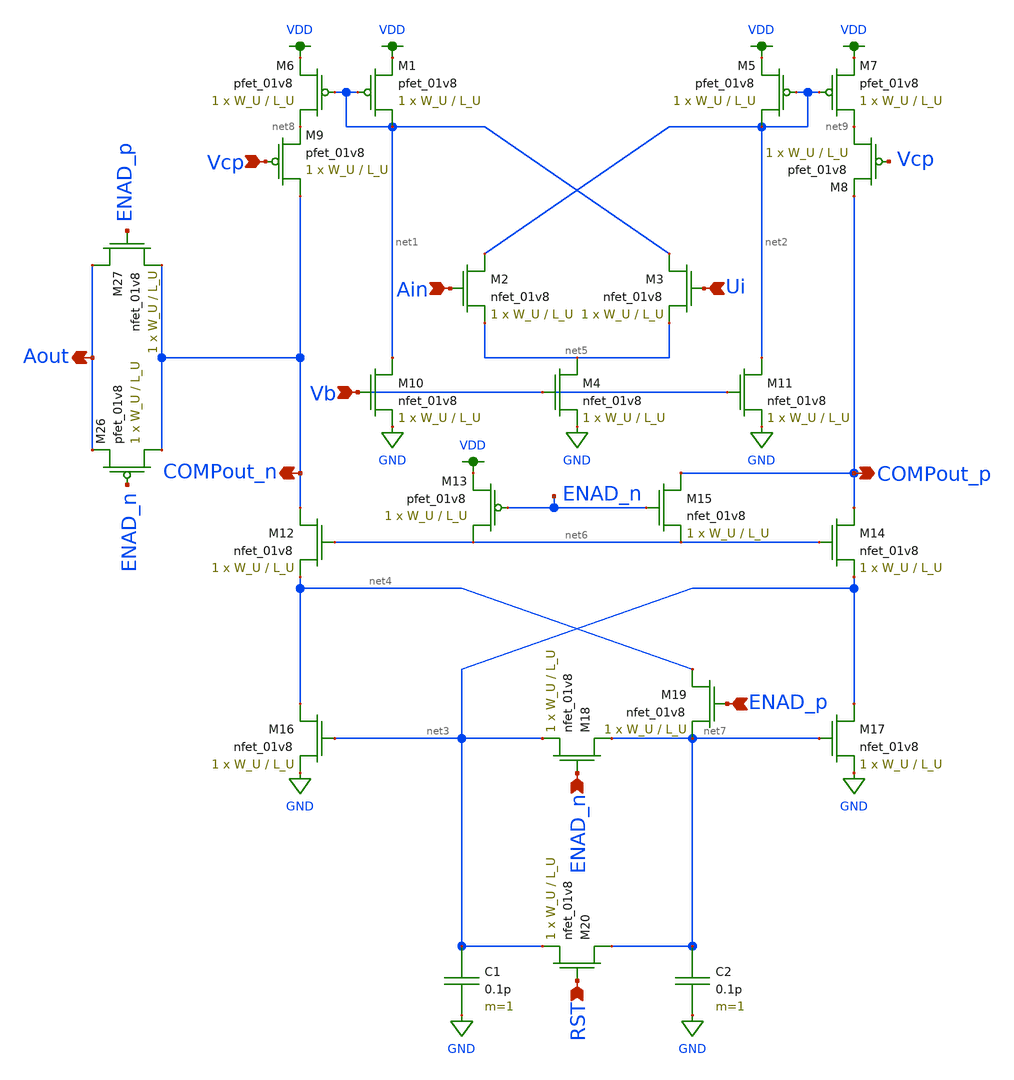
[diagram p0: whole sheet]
** sch_path: schematics/comp_pretty.sch
**.subckt comp_pretty Ain Vcp Vb Aout COMPout_n COMPout_p ENAD_n RST Ui ENAD_p
*.ipin Ain
*.ipin Vcp
*.ipin Vb
*.opin Aout
*.opin COMPout_n
*.opin COMPout_p
*.ipin ENAD_n
*.ipin RST
*.ipin Ui
*.ipin ENAD_p
XM1 net1 net1 VDD VDD sky130_fd_pr__pfet_01v8 L=L_U W=W_U nf=1 ad='int((nf+1)/2) * W/nf * 0.29' as='int((nf+2)/2) * W/nf * 0.29'
+ pd='2*int((nf+1)/2) * (W/nf + 0.29)' ps='2*int((nf+2)/2) * (W/nf + 0.29)' nrd='0.29 / W' nrs='0.29 / W'
+ sa=0 sb=0 sd=0 mult=1 m=1
XM2 net2 Ain net5 GND sky130_fd_pr__nfet_01v8 L=L_U W=W_U nf=1 ad='int((nf+1)/2) * W/nf * 0.29' as='int((nf+2)/2) * W/nf * 0.29'
+ pd='2*int((nf+1)/2) * (W/nf + 0.29)' ps='2*int((nf+2)/2) * (W/nf + 0.29)' nrd='0.29 / W' nrs='0.29 / W'
+ sa=0 sb=0 sd=0 mult=1 m=1
XM3 net1 Ui net5 GND sky130_fd_pr__nfet_01v8 L=L_U W=W_U nf=1 ad='int((nf+1)/2) * W/nf * 0.29' as='int((nf+2)/2) * W/nf * 0.29'
+ pd='2*int((nf+1)/2) * (W/nf + 0.29)' ps='2*int((nf+2)/2) * (W/nf + 0.29)' nrd='0.29 / W' nrs='0.29 / W'
+ sa=0 sb=0 sd=0 mult=1 m=1
XM4 net5 Vb GND GND sky130_fd_pr__nfet_01v8 L=L_U W=W_U nf=1 ad='int((nf+1)/2) * W/nf * 0.29' as='int((nf+2)/2) * W/nf * 0.29'
+ pd='2*int((nf+1)/2) * (W/nf + 0.29)' ps='2*int((nf+2)/2) * (W/nf + 0.29)' nrd='0.29 / W' nrs='0.29 / W'
+ sa=0 sb=0 sd=0 mult=1 m=1
XM5 net2 net2 VDD VDD sky130_fd_pr__pfet_01v8 L=L_U W=W_U nf=1 ad='int((nf+1)/2) * W/nf * 0.29' as='int((nf+2)/2) * W/nf * 0.29'
+ pd='2*int((nf+1)/2) * (W/nf + 0.29)' ps='2*int((nf+2)/2) * (W/nf + 0.29)' nrd='0.29 / W' nrs='0.29 / W'
+ sa=0 sb=0 sd=0 mult=1 m=1
XM6 net8 net1 VDD VDD sky130_fd_pr__pfet_01v8 L=L_U W=W_U nf=1 ad='int((nf+1)/2) * W/nf * 0.29' as='int((nf+2)/2) * W/nf * 0.29'
+ pd='2*int((nf+1)/2) * (W/nf + 0.29)' ps='2*int((nf+2)/2) * (W/nf + 0.29)' nrd='0.29 / W' nrs='0.29 / W'
+ sa=0 sb=0 sd=0 mult=1 m=1
XM7 net9 net2 VDD VDD sky130_fd_pr__pfet_01v8 L=L_U W=W_U nf=1 ad='int((nf+1)/2) * W/nf * 0.29' as='int((nf+2)/2) * W/nf * 0.29'
+ pd='2*int((nf+1)/2) * (W/nf + 0.29)' ps='2*int((nf+2)/2) * (W/nf + 0.29)' nrd='0.29 / W' nrs='0.29 / W'
+ sa=0 sb=0 sd=0 mult=1 m=1
XM8 net9 Vcp COMPout_p VDD sky130_fd_pr__pfet_01v8 L=L_U W=W_U nf=1 ad='int((nf+1)/2) * W/nf * 0.29'
+ as='int((nf+2)/2) * W/nf * 0.29' pd='2*int((nf+1)/2) * (W/nf + 0.29)' ps='2*int((nf+2)/2) * (W/nf + 0.29)'
+ nrd='0.29 / W' nrs='0.29 / W' sa=0 sb=0 sd=0 mult=1 m=1
XM9 COMPout_n Vcp net8 VDD sky130_fd_pr__pfet_01v8 L=L_U W=W_U nf=1 ad='int((nf+1)/2) * W/nf * 0.29'
+ as='int((nf+2)/2) * W/nf * 0.29' pd='2*int((nf+1)/2) * (W/nf + 0.29)' ps='2*int((nf+2)/2) * (W/nf + 0.29)'
+ nrd='0.29 / W' nrs='0.29 / W' sa=0 sb=0 sd=0 mult=1 m=1
XM10 net1 Vb GND GND sky130_fd_pr__nfet_01v8 L=L_U W=W_U nf=1 ad='int((nf+1)/2) * W/nf * 0.29' as='int((nf+2)/2) * W/nf * 0.29'
+ pd='2*int((nf+1)/2) * (W/nf + 0.29)' ps='2*int((nf+2)/2) * (W/nf + 0.29)' nrd='0.29 / W' nrs='0.29 / W'
+ sa=0 sb=0 sd=0 mult=1 m=1
XM11 net2 Vb GND GND sky130_fd_pr__nfet_01v8 L=L_U W=W_U nf=1 ad='int((nf+1)/2) * W/nf * 0.29' as='int((nf+2)/2) * W/nf * 0.29'
+ pd='2*int((nf+1)/2) * (W/nf + 0.29)' ps='2*int((nf+2)/2) * (W/nf + 0.29)' nrd='0.29 / W' nrs='0.29 / W'
+ sa=0 sb=0 sd=0 mult=1 m=1
XM12 COMPout_n net6 net4 GND sky130_fd_pr__nfet_01v8 L=L_U W=W_U nf=1 ad='int((nf+1)/2) * W/nf * 0.29'
+ as='int((nf+2)/2) * W/nf * 0.29' pd='2*int((nf+1)/2) * (W/nf + 0.29)' ps='2*int((nf+2)/2) * (W/nf + 0.29)'
+ nrd='0.29 / W' nrs='0.29 / W' sa=0 sb=0 sd=0 mult=1 m=1
XM13 net6 ENAD_n VDD VDD sky130_fd_pr__pfet_01v8 L=L_U W=W_U nf=1 ad='int((nf+1)/2) * W/nf * 0.29' as='int((nf+2)/2) * W/nf * 0.29'
+ pd='2*int((nf+1)/2) * (W/nf + 0.29)' ps='2*int((nf+2)/2) * (W/nf + 0.29)' nrd='0.29 / W' nrs='0.29 / W'
+ sa=0 sb=0 sd=0 mult=1 m=1
XM14 COMPout_p net6 net3 GND sky130_fd_pr__nfet_01v8 L=L_U W=W_U nf=1 ad='int((nf+1)/2) * W/nf * 0.29'
+ as='int((nf+2)/2) * W/nf * 0.29' pd='2*int((nf+1)/2) * (W/nf + 0.29)' ps='2*int((nf+2)/2) * (W/nf + 0.29)'
+ nrd='0.29 / W' nrs='0.29 / W' sa=0 sb=0 sd=0 mult=1 m=1
XM15 COMPout_p ENAD_n net6 GND sky130_fd_pr__nfet_01v8 L=L_U W=W_U nf=1 ad='int((nf+1)/2) * W/nf * 0.29'
+ as='int((nf+2)/2) * W/nf * 0.29' pd='2*int((nf+1)/2) * (W/nf + 0.29)' ps='2*int((nf+2)/2) * (W/nf + 0.29)'
+ nrd='0.29 / W' nrs='0.29 / W' sa=0 sb=0 sd=0 mult=1 m=1
XM16 net4 net3 GND GND sky130_fd_pr__nfet_01v8 L=L_U W=W_U nf=1 ad='int((nf+1)/2) * W/nf * 0.29' as='int((nf+2)/2) * W/nf * 0.29'
+ pd='2*int((nf+1)/2) * (W/nf + 0.29)' ps='2*int((nf+2)/2) * (W/nf + 0.29)' nrd='0.29 / W' nrs='0.29 / W'
+ sa=0 sb=0 sd=0 mult=1 m=1
XM17 net3 net7 GND GND sky130_fd_pr__nfet_01v8 L=L_U W=W_U nf=1 ad='int((nf+1)/2) * W/nf * 0.29' as='int((nf+2)/2) * W/nf * 0.29'
+ pd='2*int((nf+1)/2) * (W/nf + 0.29)' ps='2*int((nf+2)/2) * (W/nf + 0.29)' nrd='0.29 / W' nrs='0.29 / W'
+ sa=0 sb=0 sd=0 mult=1 m=1
XM18 net7 ENAD_n net3 GND sky130_fd_pr__nfet_01v8 L=L_U W=W_U nf=1 ad='int((nf+1)/2) * W/nf * 0.29' as='int((nf+2)/2) * W/nf * 0.29'
+ pd='2*int((nf+1)/2) * (W/nf + 0.29)' ps='2*int((nf+2)/2) * (W/nf + 0.29)' nrd='0.29 / W' nrs='0.29 / W'
+ sa=0 sb=0 sd=0 mult=1 m=1
XM19 net4 ENAD_p net7 GND sky130_fd_pr__nfet_01v8 L=L_U W=W_U nf=1 ad='int((nf+1)/2) * W/nf * 0.29' as='int((nf+2)/2) * W/nf * 0.29'
+ pd='2*int((nf+1)/2) * (W/nf + 0.29)' ps='2*int((nf+2)/2) * (W/nf + 0.29)' nrd='0.29 / W' nrs='0.29 / W'
+ sa=0 sb=0 sd=0 mult=1 m=1
XM20 net7 RST net3 GND sky130_fd_pr__nfet_01v8 L=L_U W=W_U nf=1 ad='int((nf+1)/2) * W/nf * 0.29' as='int((nf+2)/2) * W/nf * 0.29'
+ pd='2*int((nf+1)/2) * (W/nf + 0.29)' ps='2*int((nf+2)/2) * (W/nf + 0.29)' nrd='0.29 / W' nrs='0.29 / W'
+ sa=0 sb=0 sd=0 mult=1 m=1
C1 net3 GND 0.1p m=1
C2 net7 GND 0.1p m=1
XM26 COMPout_n ENAD_n Aout VDD sky130_fd_pr__pfet_01v8 L=L_U W=W_U nf=1 ad='int((nf+1)/2) * W/nf * 0.29'
+ as='int((nf+2)/2) * W/nf * 0.29' pd='2*int((nf+1)/2) * (W/nf + 0.29)' ps='2*int((nf+2)/2) * (W/nf + 0.29)'
+ nrd='0.29 / W' nrs='0.29 / W' sa=0 sb=0 sd=0 mult=1 m=1
XM27 Aout ENAD_p COMPout_n GND sky130_fd_pr__nfet_01v8 L=L_U W=W_U nf=1 ad='int((nf+1)/2) * W/nf * 0.29'
+ as='int((nf+2)/2) * W/nf * 0.29' pd='2*int((nf+1)/2) * (W/nf + 0.29)' ps='2*int((nf+2)/2) * (W/nf + 0.29)'
+ nrd='0.29 / W' nrs='0.29 / W' sa=0 sb=0 sd=0 mult=1 m=1
**.ends
.GLOBAL VDD
.GLOBAL GND
.end
